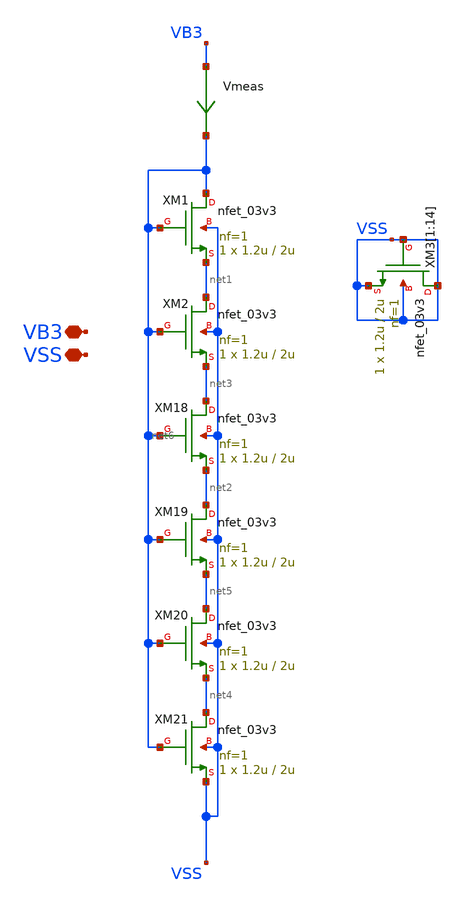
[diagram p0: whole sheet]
** sch_path: TIA_Filter/Folded/FC_bias_vb3.sch
**.subckt FC_bias_vb3 VSS VB3
*.iopin VSS
*.iopin VB3
XM1 net6 net6 net1 VSS nfet_03v3 L=2u W=1.2u nf=1 ad='int((nf+1)/2) * W/nf * 0.18u' as='int((nf+2)/2) * W/nf * 0.18u'
+ pd='2*int((nf+1)/2) * (W/nf + 0.18u)' ps='2*int((nf+2)/2) * (W/nf + 0.18u)' nrd='0.18u / W' nrs='0.18u / W'
+ sa=0 sb=0 sd=0 m=1
XM2 net1 net6 net3 VSS nfet_03v3 L=2u W=1.2u nf=1 ad='int((nf+1)/2) * W/nf * 0.18u' as='int((nf+2)/2) * W/nf * 0.18u'
+ pd='2*int((nf+1)/2) * (W/nf + 0.18u)' ps='2*int((nf+2)/2) * (W/nf + 0.18u)' nrd='0.18u / W' nrs='0.18u / W'
+ sa=0 sb=0 sd=0 m=1
XM18 net3 net6 net2 VSS nfet_03v3 L=2u W=1.2u nf=1 ad='int((nf+1)/2) * W/nf * 0.18u' as='int((nf+2)/2) * W/nf * 0.18u'
+ pd='2*int((nf+1)/2) * (W/nf + 0.18u)' ps='2*int((nf+2)/2) * (W/nf + 0.18u)' nrd='0.18u / W' nrs='0.18u / W'
+ sa=0 sb=0 sd=0 m=1
XM19 net2 net6 net5 VSS nfet_03v3 L=2u W=1.2u nf=1 ad='int((nf+1)/2) * W/nf * 0.18u' as='int((nf+2)/2) * W/nf * 0.18u'
+ pd='2*int((nf+1)/2) * (W/nf + 0.18u)' ps='2*int((nf+2)/2) * (W/nf + 0.18u)' nrd='0.18u / W' nrs='0.18u / W'
+ sa=0 sb=0 sd=0 m=1
XM20 net5 net6 net4 VSS nfet_03v3 L=2u W=1.2u nf=1 ad='int((nf+1)/2) * W/nf * 0.18u' as='int((nf+2)/2) * W/nf * 0.18u'
+ pd='2*int((nf+1)/2) * (W/nf + 0.18u)' ps='2*int((nf+2)/2) * (W/nf + 0.18u)' nrd='0.18u / W' nrs='0.18u / W'
+ sa=0 sb=0 sd=0 m=1
XM21 net4 net6 VSS VSS nfet_03v3 L=2u W=1.2u nf=1 ad='int((nf+1)/2) * W/nf * 0.18u' as='int((nf+2)/2) * W/nf * 0.18u'
+ pd='2*int((nf+1)/2) * (W/nf + 0.18u)' ps='2*int((nf+2)/2) * (W/nf + 0.18u)' nrd='0.18u / W' nrs='0.18u / W'
+ sa=0 sb=0 sd=0 m=1
XM3[1] VSS VSS VSS VSS nfet_03v3 L=2u W=1.2u nf=1 ad='int((nf+1)/2) * W/nf * 0.18u' as='int((nf+2)/2) * W/nf * 0.18u'
+ pd='2*int((nf+1)/2) * (W/nf + 0.18u)' ps='2*int((nf+2)/2) * (W/nf + 0.18u)' nrd='0.18u / W' nrs='0.18u / W'
+ sa=0 sb=0 sd=0 m=1
XM3[2] VSS VSS VSS VSS nfet_03v3 L=2u W=1.2u nf=1 ad='int((nf+1)/2) * W/nf * 0.18u' as='int((nf+2)/2) * W/nf * 0.18u'
+ pd='2*int((nf+1)/2) * (W/nf + 0.18u)' ps='2*int((nf+2)/2) * (W/nf + 0.18u)' nrd='0.18u / W' nrs='0.18u / W'
+ sa=0 sb=0 sd=0 m=1
XM3[3] VSS VSS VSS VSS nfet_03v3 L=2u W=1.2u nf=1 ad='int((nf+1)/2) * W/nf * 0.18u' as='int((nf+2)/2) * W/nf * 0.18u'
+ pd='2*int((nf+1)/2) * (W/nf + 0.18u)' ps='2*int((nf+2)/2) * (W/nf + 0.18u)' nrd='0.18u / W' nrs='0.18u / W'
+ sa=0 sb=0 sd=0 m=1
XM3[4] VSS VSS VSS VSS nfet_03v3 L=2u W=1.2u nf=1 ad='int((nf+1)/2) * W/nf * 0.18u' as='int((nf+2)/2) * W/nf * 0.18u'
+ pd='2*int((nf+1)/2) * (W/nf + 0.18u)' ps='2*int((nf+2)/2) * (W/nf + 0.18u)' nrd='0.18u / W' nrs='0.18u / W'
+ sa=0 sb=0 sd=0 m=1
XM3[5] VSS VSS VSS VSS nfet_03v3 L=2u W=1.2u nf=1 ad='int((nf+1)/2) * W/nf * 0.18u' as='int((nf+2)/2) * W/nf * 0.18u'
+ pd='2*int((nf+1)/2) * (W/nf + 0.18u)' ps='2*int((nf+2)/2) * (W/nf + 0.18u)' nrd='0.18u / W' nrs='0.18u / W'
+ sa=0 sb=0 sd=0 m=1
XM3[6] VSS VSS VSS VSS nfet_03v3 L=2u W=1.2u nf=1 ad='int((nf+1)/2) * W/nf * 0.18u' as='int((nf+2)/2) * W/nf * 0.18u'
+ pd='2*int((nf+1)/2) * (W/nf + 0.18u)' ps='2*int((nf+2)/2) * (W/nf + 0.18u)' nrd='0.18u / W' nrs='0.18u / W'
+ sa=0 sb=0 sd=0 m=1
XM3[7] VSS VSS VSS VSS nfet_03v3 L=2u W=1.2u nf=1 ad='int((nf+1)/2) * W/nf * 0.18u' as='int((nf+2)/2) * W/nf * 0.18u'
+ pd='2*int((nf+1)/2) * (W/nf + 0.18u)' ps='2*int((nf+2)/2) * (W/nf + 0.18u)' nrd='0.18u / W' nrs='0.18u / W'
+ sa=0 sb=0 sd=0 m=1
XM3[8] VSS VSS VSS VSS nfet_03v3 L=2u W=1.2u nf=1 ad='int((nf+1)/2) * W/nf * 0.18u' as='int((nf+2)/2) * W/nf * 0.18u'
+ pd='2*int((nf+1)/2) * (W/nf + 0.18u)' ps='2*int((nf+2)/2) * (W/nf + 0.18u)' nrd='0.18u / W' nrs='0.18u / W'
+ sa=0 sb=0 sd=0 m=1
XM3[9] VSS VSS VSS VSS nfet_03v3 L=2u W=1.2u nf=1 ad='int((nf+1)/2) * W/nf * 0.18u' as='int((nf+2)/2) * W/nf * 0.18u'
+ pd='2*int((nf+1)/2) * (W/nf + 0.18u)' ps='2*int((nf+2)/2) * (W/nf + 0.18u)' nrd='0.18u / W' nrs='0.18u / W'
+ sa=0 sb=0 sd=0 m=1
XM3[10] VSS VSS VSS VSS nfet_03v3 L=2u W=1.2u nf=1 ad='int((nf+1)/2) * W/nf * 0.18u' as='int((nf+2)/2) * W/nf * 0.18u'
+ pd='2*int((nf+1)/2) * (W/nf + 0.18u)' ps='2*int((nf+2)/2) * (W/nf + 0.18u)' nrd='0.18u / W' nrs='0.18u / W'
+ sa=0 sb=0 sd=0 m=1
XM3[11] VSS VSS VSS VSS nfet_03v3 L=2u W=1.2u nf=1 ad='int((nf+1)/2) * W/nf * 0.18u' as='int((nf+2)/2) * W/nf * 0.18u'
+ pd='2*int((nf+1)/2) * (W/nf + 0.18u)' ps='2*int((nf+2)/2) * (W/nf + 0.18u)' nrd='0.18u / W' nrs='0.18u / W'
+ sa=0 sb=0 sd=0 m=1
XM3[12] VSS VSS VSS VSS nfet_03v3 L=2u W=1.2u nf=1 ad='int((nf+1)/2) * W/nf * 0.18u' as='int((nf+2)/2) * W/nf * 0.18u'
+ pd='2*int((nf+1)/2) * (W/nf + 0.18u)' ps='2*int((nf+2)/2) * (W/nf + 0.18u)' nrd='0.18u / W' nrs='0.18u / W'
+ sa=0 sb=0 sd=0 m=1
XM3[13] VSS VSS VSS VSS nfet_03v3 L=2u W=1.2u nf=1 ad='int((nf+1)/2) * W/nf * 0.18u' as='int((nf+2)/2) * W/nf * 0.18u'
+ pd='2*int((nf+1)/2) * (W/nf + 0.18u)' ps='2*int((nf+2)/2) * (W/nf + 0.18u)' nrd='0.18u / W' nrs='0.18u / W'
+ sa=0 sb=0 sd=0 m=1
XM3[14] VSS VSS VSS VSS nfet_03v3 L=2u W=1.2u nf=1 ad='int((nf+1)/2) * W/nf * 0.18u' as='int((nf+2)/2) * W/nf * 0.18u'
+ pd='2*int((nf+1)/2) * (W/nf + 0.18u)' ps='2*int((nf+2)/2) * (W/nf + 0.18u)' nrd='0.18u / W' nrs='0.18u / W'
+ sa=0 sb=0 sd=0 m=1
Vmeas VB3 net6 0
.save i(vmeas)
**.ends
.end
